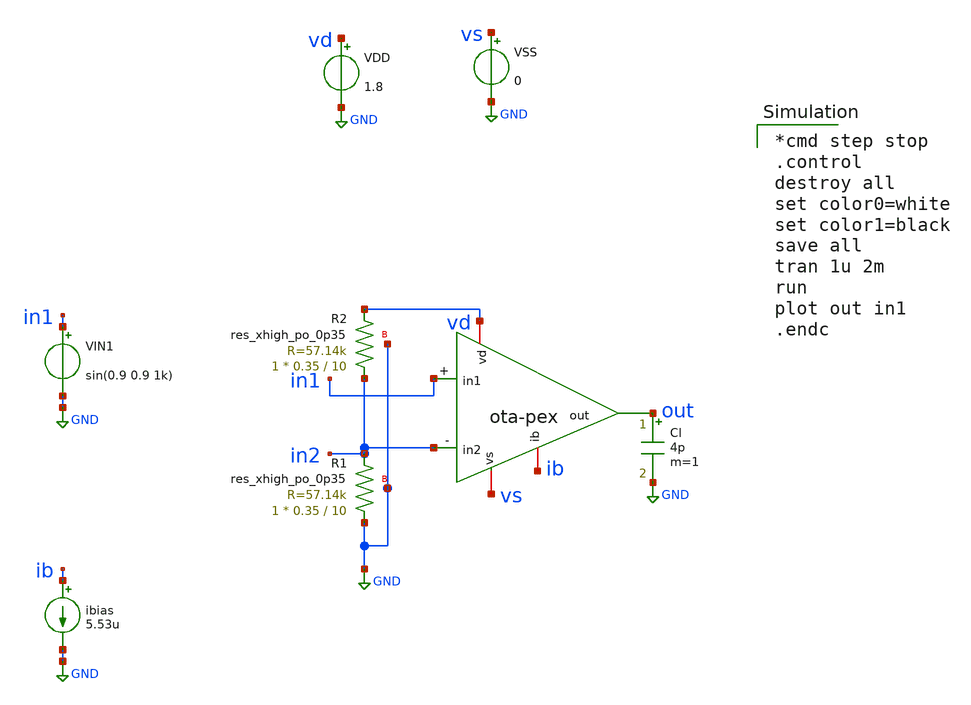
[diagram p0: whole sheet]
** sch_path: ota/xschem/ota_tb-tran.sch
* Copyright 2020 Stefan Frederik Schippers
* Licensed under the Apache License, Version 2.0 (the "License");
* you may not use this file except in compliance with the License.
* You may obtain a copy of the License at
* https://www.apache.org/licenses/LICENSE-2.0
* Unless required by applicable law or agreed to in writing, software
* distributed under the License is distributed on an "AS IS" BASIS,
* WITHOUT WARRANTIES OR CONDITIONS OF ANY KIND, either express or implied.
* See the License for the specific language governing permissions and
* limitations under the License.
**.subckt ota_tb-tran
VIN1 in1 GND sin(0.9 0.9 1k)
ibias ib GND 5.53u
VDD vd GND 1.8
VSS vs GND 0
Cl out GND 4p m=1
XR1 GND in2 GND sky130_fd_pr__res_xhigh_po_0p35 L=10 mult=1 m=1
XR2 in2 vd GND sky130_fd_pr__res_xhigh_po_0p35 L=10 mult=1 m=1
X1 vd ib out in2 in1 vs ota-pex
**** begin user architecture code

*cmd step stop
.control
destroy all
set color0=white
set color1=black
save all
tran 1u 2m
run
plot out in1
.endc

 .lib $::SKYWATER_MODELS/sky130.lib.spice tt
.include $::SKYWATER_STDCELLS/sky130_fd_sc_hd.spice

**** end user architecture code
**.ends
.GLOBAL GND
.end
